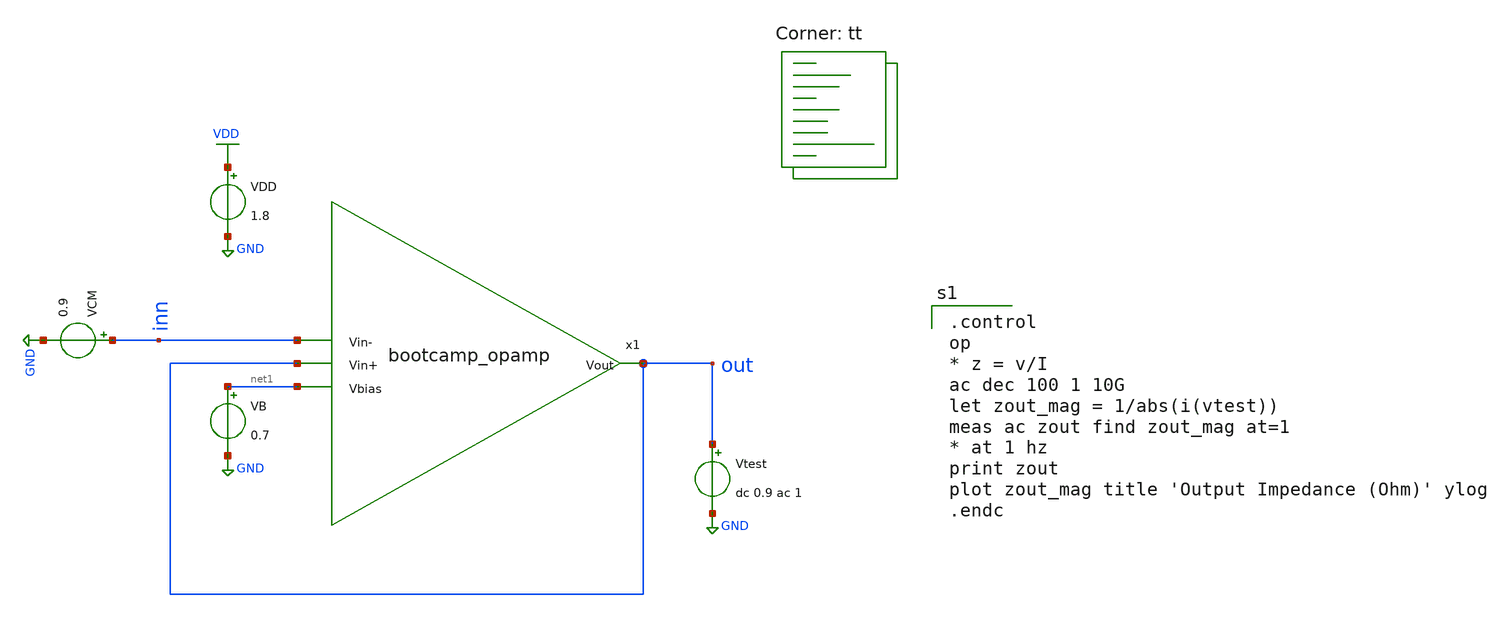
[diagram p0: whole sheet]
** sch_path: analog/schematics/tb_output_impedance.sch
**.subckt tb_output_impedance
x1 out inn out net1 bootcamp_opamp
VDD VDD GND 1.8
VB net1 GND 0.7
VCM inn GND 0.9
Vtest out GND dc 0.9 ac 1
**** begin user architecture code
.lib $::SKYWATER_MODELS/sky130.lib.spice tt

.control
op
* z = v/I
ac dec 100 1 10G
let zout_mag = 1/abs(i(vtest))
meas ac zout find zout_mag at=1
* at 1 hz
print zout
plot zout_mag title 'Output Impedance (Ohm)' ylog
.endc

**** end user architecture code
**.ends
.GLOBAL GND
.GLOBAL VDD
.end
